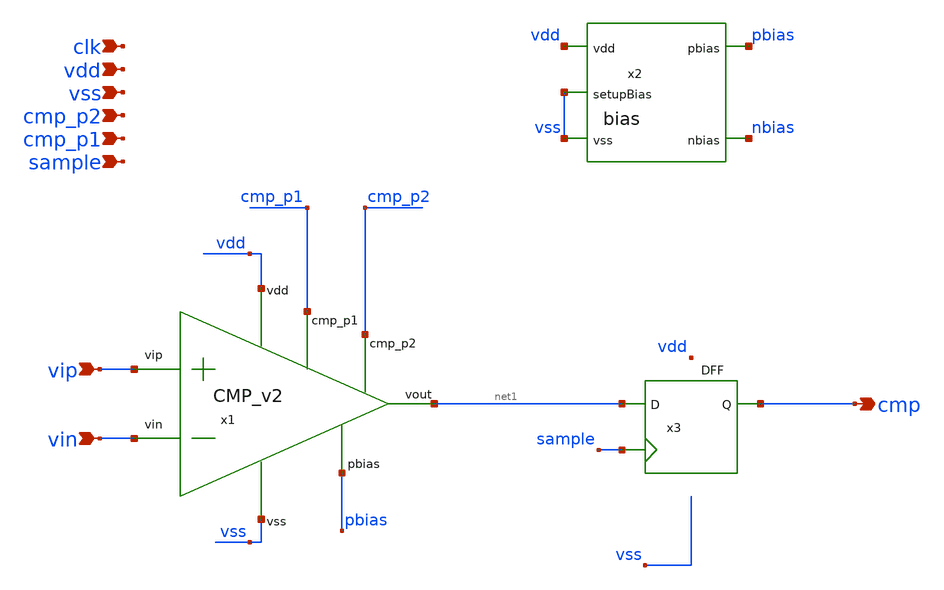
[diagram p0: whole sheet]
** sch_path: design/JNW_AVV_SKY130A/TB_CMP.sch
**.subckt TB_CMP vdd vss vip vin cmp cmp_p1 cmp_p2 clk sample
*.ipin vdd
*.ipin vss
*.ipin vip
*.ipin vin
*.opin cmp
*.ipin cmp_p1
*.ipin cmp_p2
*.ipin clk
*.ipin sample
x2 pbias vdd nbias vss vss bias
x3 cmp net1 sample VCC VSS VCC VSS DFF
x1 vdd pbias net1 vin vip vss cmp_p1 cmp_p2 CMP_v2
**.ends
.end
